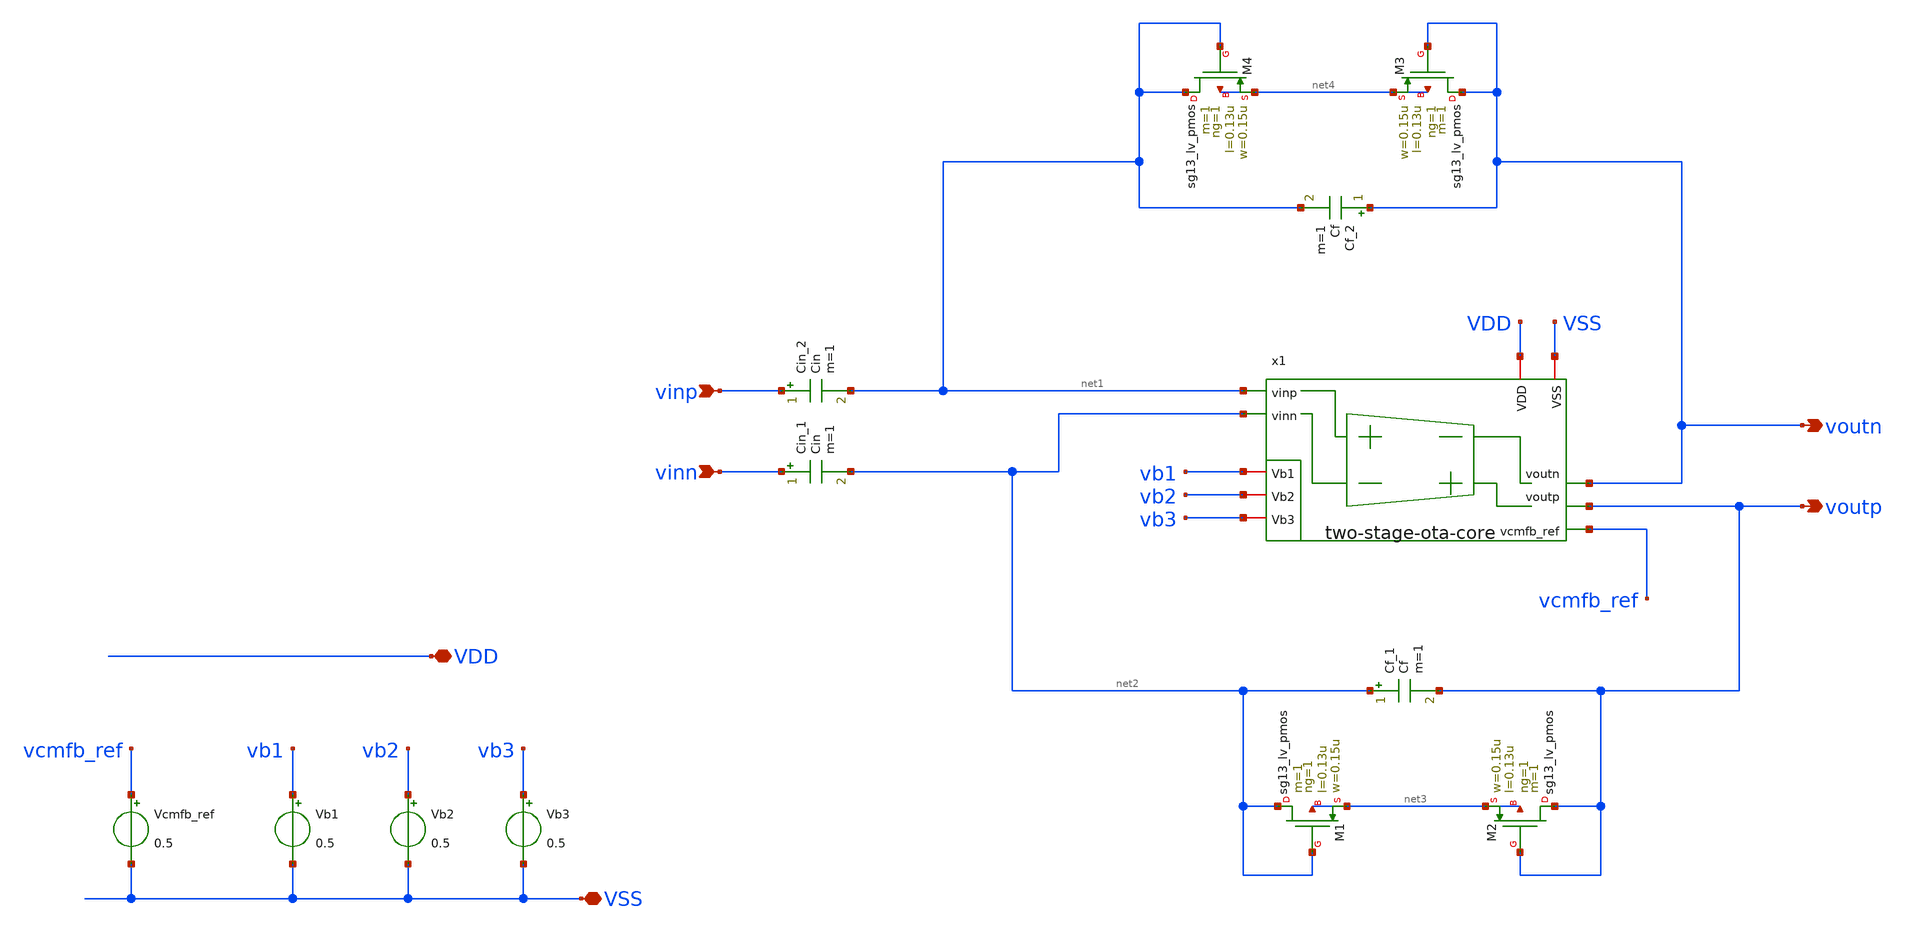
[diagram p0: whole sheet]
** sch_path: analog-db/drawings/ccia-01-YuPinHsu-bandpass-class-ab-output/ccia-dut.sch
* Copyright 2026 MacAnalog Research Group
**.subckt ccia-dut VSS VDD vinp vinn voutn voutp
*.iopin VSS
*.iopin VDD
*.ipin vinp
*.ipin vinn
*.opin voutn
*.opin voutp
x1 vb1 net1 vb2 net2 vb3 voutn voutp VSS VDD vcmfb_ref two-stage-ota-core
Vb1 vb1 VSS 0.5
Vb2 vb2 VSS 0.5
Vb3 vb3 VSS 0.5
Vcmfb_ref vcmfb_ref VSS 0.5
Cin_2 vinp net1 Cin m=1
XM1 net2 net2 net3 net3 sg13_lv_pmos w=0.15u l=0.13u ng=1 m=1 mm_ok=1
XM2 voutp voutp net3 net3 sg13_lv_pmos w=0.15u l=0.13u ng=1 m=1 mm_ok=1
Cin_1 vinn net2 Cin m=1
Cf_1 net2 voutp Cf m=1
XM3 voutn voutn net4 net4 sg13_lv_pmos w=0.15u l=0.13u ng=1 m=1 mm_ok=1
XM4 net1 net1 net4 net4 sg13_lv_pmos w=0.15u l=0.13u ng=1 m=1 mm_ok=1
Cf_2 voutn net1 Cf m=1
**.ends
.end
